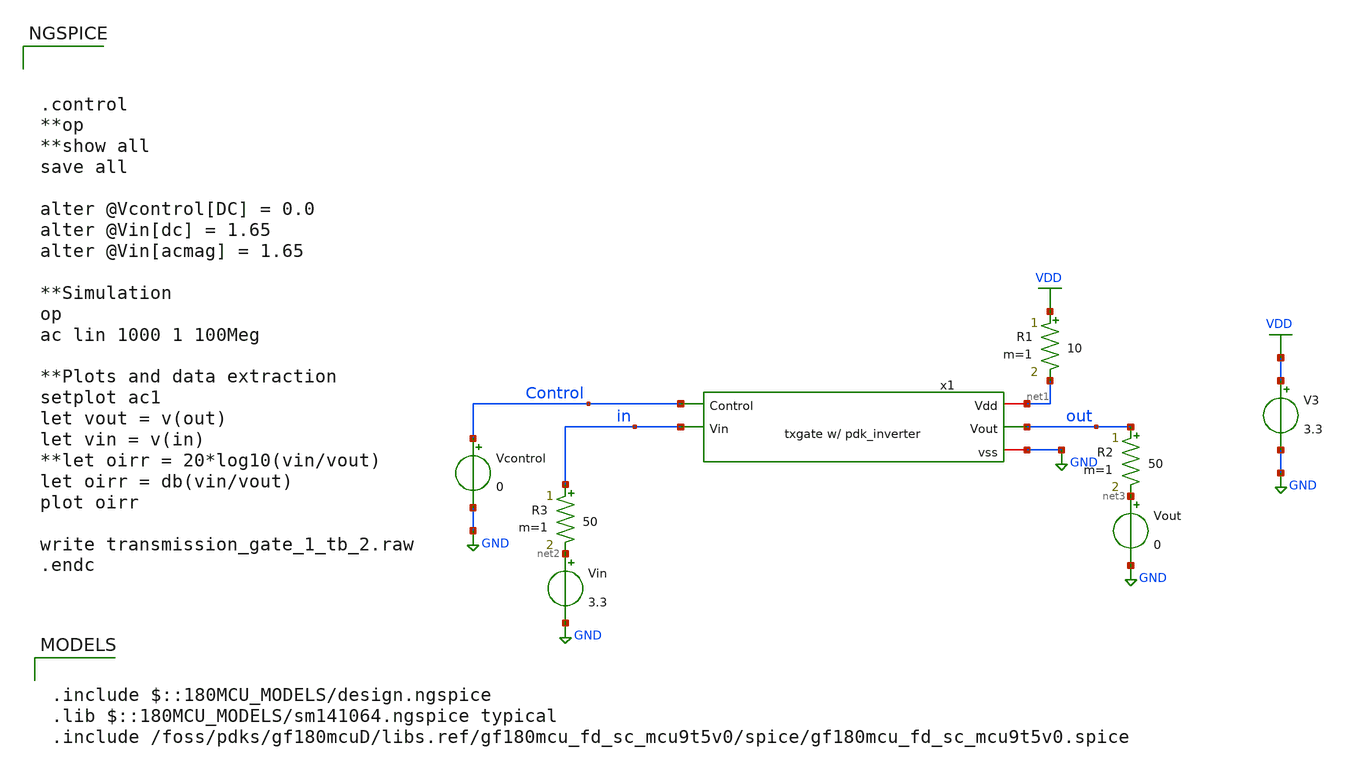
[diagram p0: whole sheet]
** sch_path: designs/transmission_gate_1_tb_2.sch
**.subckt transmission_gate_1_tb_2
Vin net2 GND 3.3
Vcontrol Control GND 0
V3 VDD GND 3.3
Vout net3 GND 0
R1 VDD net1 10 m=1
R2 out net3 50 m=1
R3 in net2 50 m=1
x1 net1 Control out in GND transmission_gate_2
**** begin user architecture code

.include $::180MCU_MODELS/design.ngspice
.lib $::180MCU_MODELS/sm141064.ngspice typical
.include /foss/pdks/gf180mcuD/libs.ref/gf180mcu_fd_sc_mcu9t5v0/spice/gf180mcu_fd_sc_mcu9t5v0.spice





.control
**op
**show all
save all

alter @Vcontrol[DC] = 0.0
alter @Vin[dc] = 1.65
alter @Vin[acmag] = 1.65

**Simulation
op
ac lin 1000 1 100Meg

**Plots and data extraction
setplot ac1
let vout = v(out)
let vin = v(in)
**let oirr = 20*log10(vin/vout)
let oirr = db(vin/vout)
plot oirr

write transmission_gate_1_tb_2.raw
.endc


**** end user architecture code
**.ends

* expanding   symbol:  libs/core_analog/tx_gate/transmission_gate_2.sym # of pins=5
** sym_path: designs/libs/core_analog/tx_gate/transmission_gate_2.sym
** sch_path: designs/libs/core_analog/tx_gate/transmission_gate_2.sch
.subckt transmission_gate_2 Vdd Control Vout Vin vss
*.iopin Vdd
*.ipin Control
*.opin Vout
*.ipin Vin
*.iopin vss
XM3 Vout Control Vin vss nfet_03v3 L=0.28u W=6u nf=1 ad='int((nf+1)/2) * W/nf * 0.18u' as='int((nf+2)/2) * W/nf * 0.18u'
+ pd='2*int((nf+1)/2) * (W/nf + 0.18u)' ps='2*int((nf+2)/2) * (W/nf + 0.18u)' nrd='0.18u / W' nrs='0.18u / W'
+ sa=0 sb=0 sd=0 m=4
XM4 Vout net1 Vin Vdd pfet_03v3 L=0.28u W=6u nf=1 ad='int((nf+1)/2) * W/nf * 0.18u' as='int((nf+2)/2) * W/nf * 0.18u'
+ pd='2*int((nf+1)/2) * (W/nf + 0.18u)' ps='2*int((nf+2)/2) * (W/nf + 0.18u)' nrd='0.18u / W' nrs='0.18u / W'
+ sa=0 sb=0 sd=0 m=12
x1 Control VSSd VDDd VSSd VDDd net1 gf180mcu_fd_sc_mcu9t5v0__inv_1
**** begin user architecture code

.include $::180MCU_MODELS/design.ngspice
.include /foss/pdks/gf180mcuD/libs.ref/gf180mcu_fd_sc_mcu9t5v0/spice/gf180mcu_fd_sc_mcu9t5v0.spice
.lib $::180MCU_MODELS/sm141064.ngspice typical

**** end user architecture code
.ends

.GLOBAL VDD
.GLOBAL GND
.end
